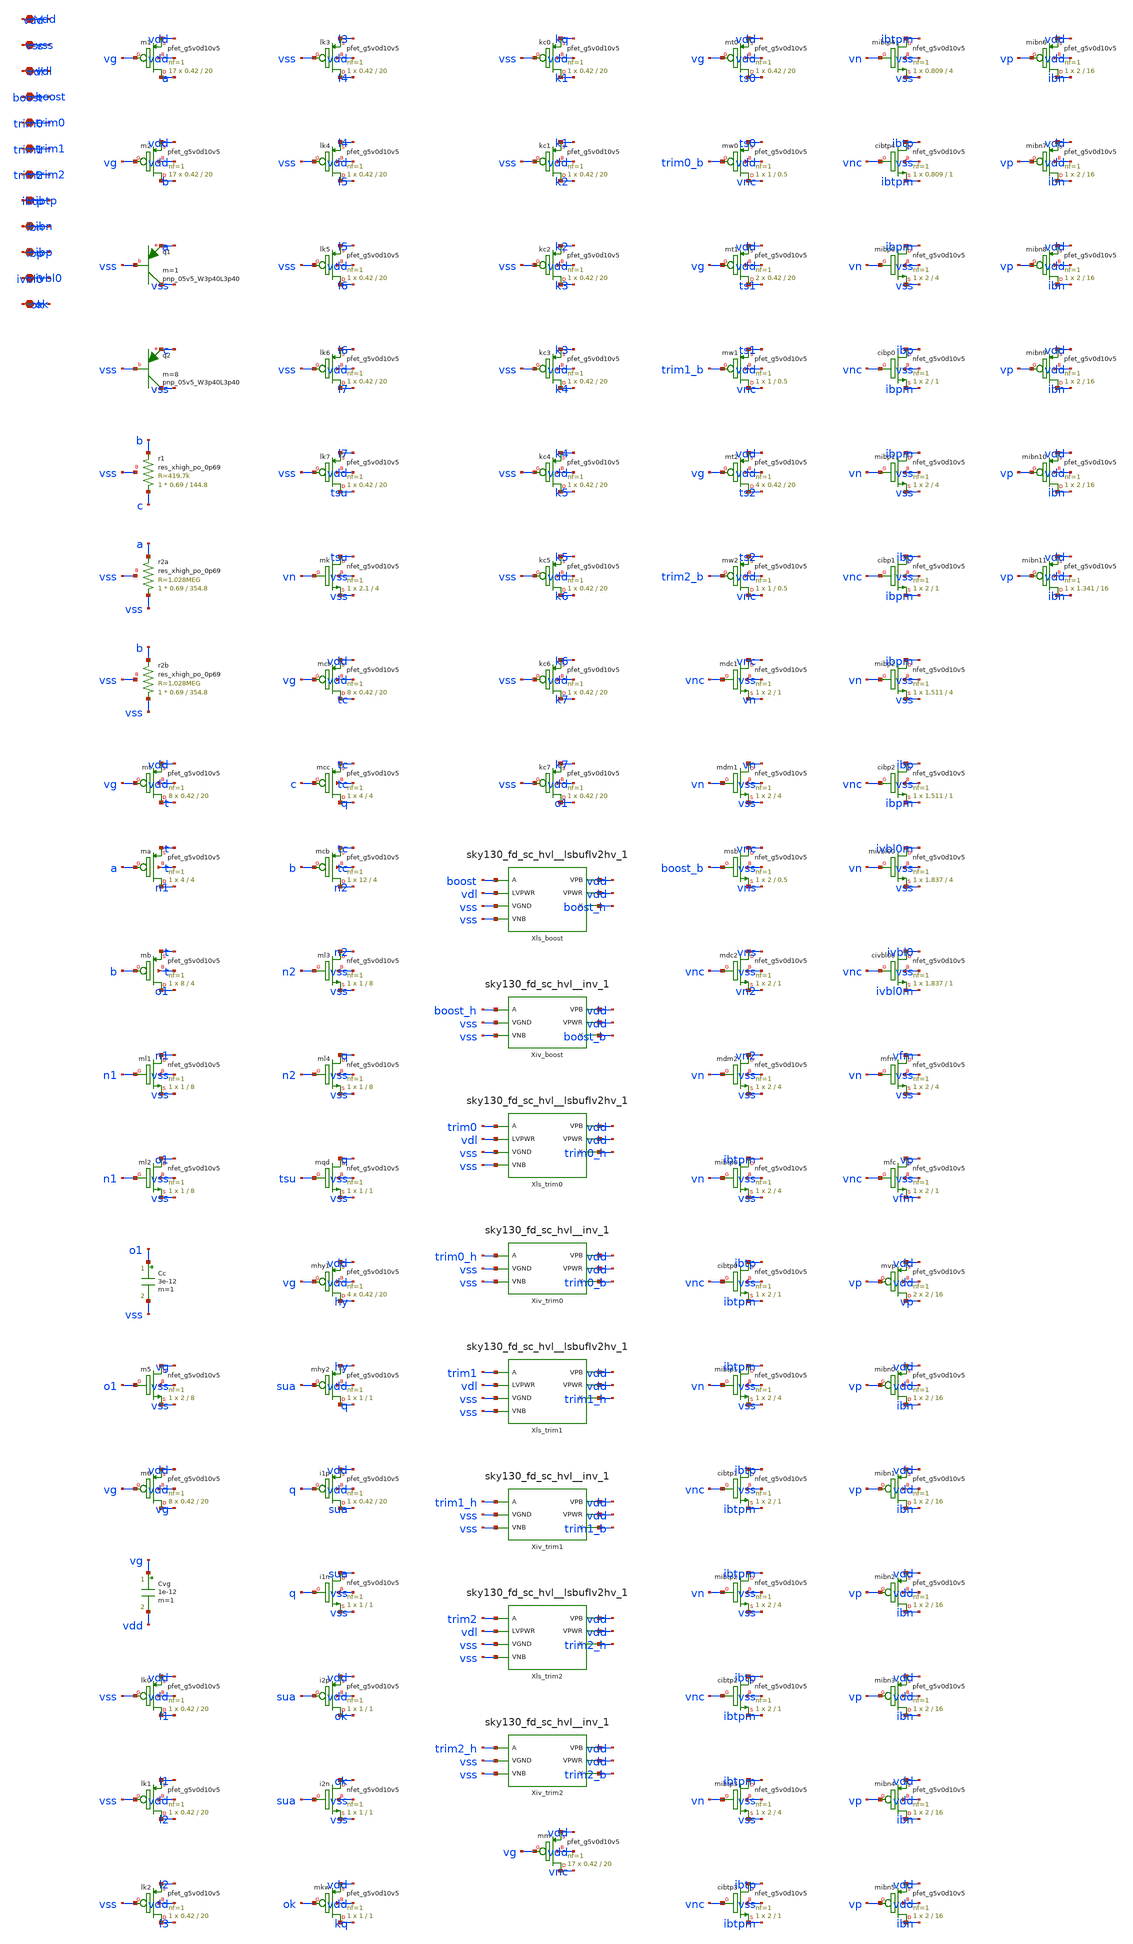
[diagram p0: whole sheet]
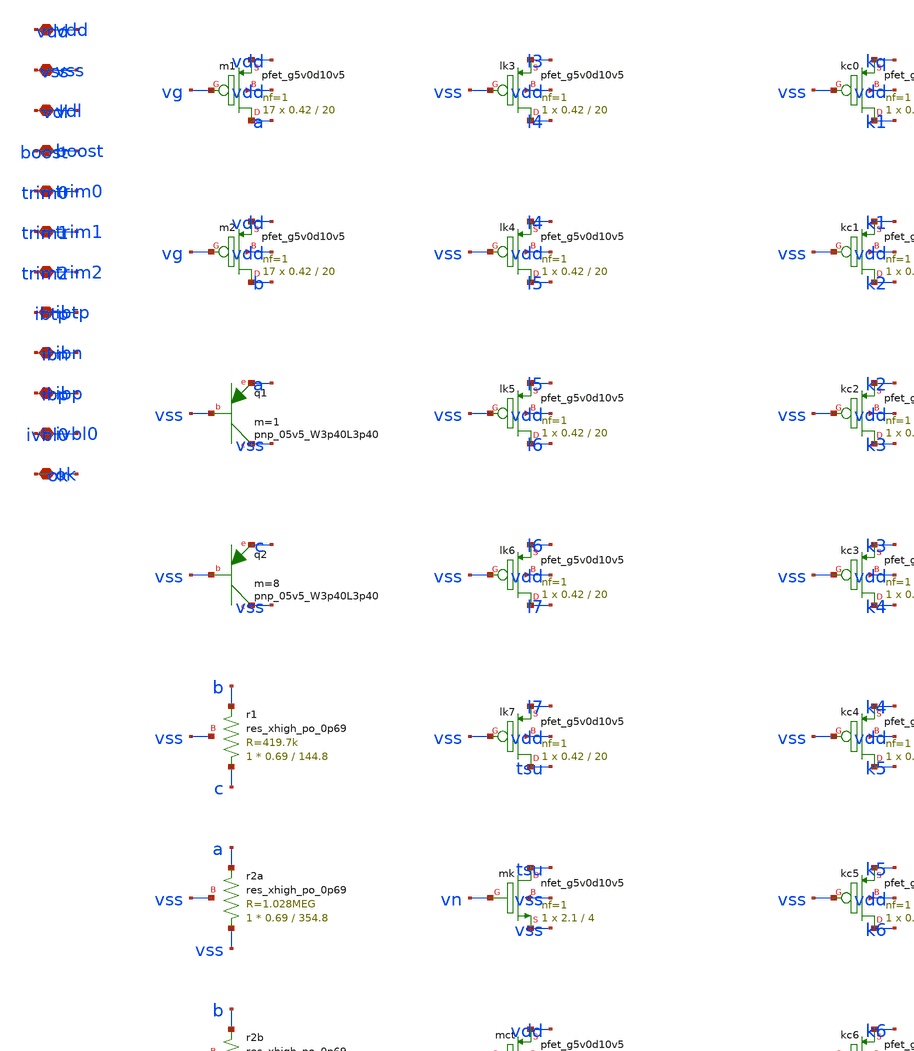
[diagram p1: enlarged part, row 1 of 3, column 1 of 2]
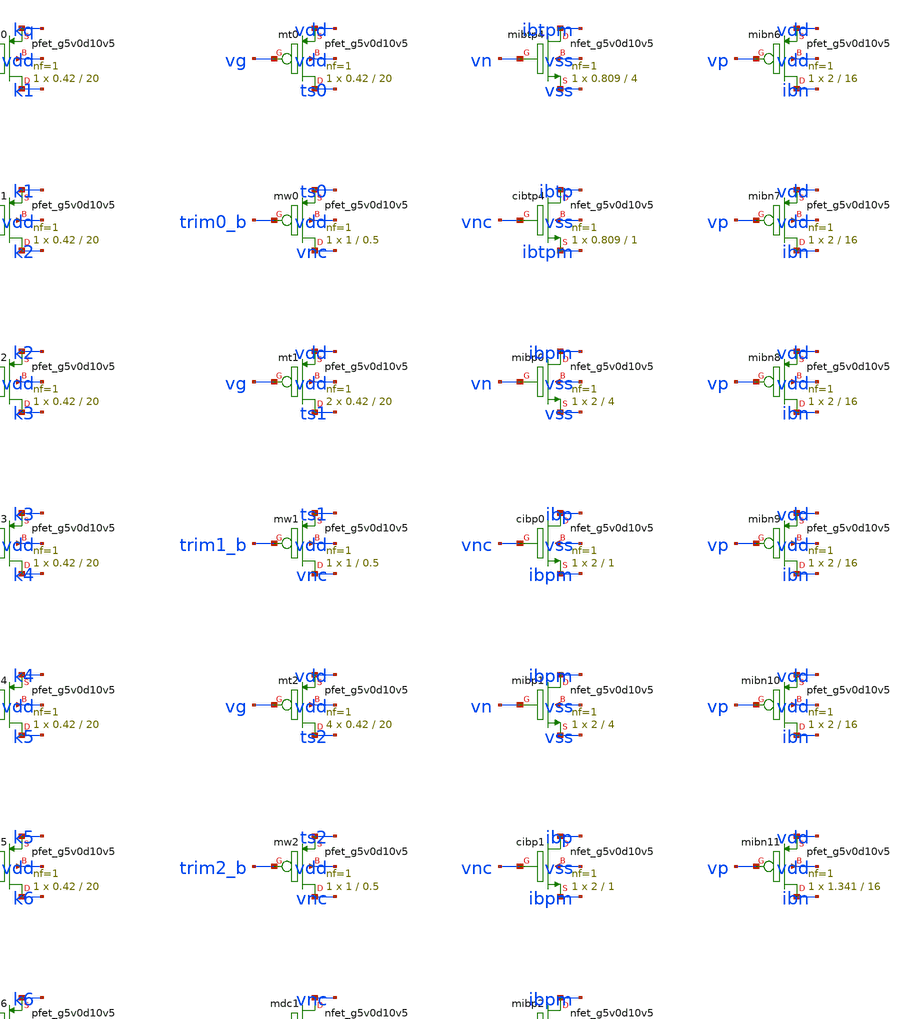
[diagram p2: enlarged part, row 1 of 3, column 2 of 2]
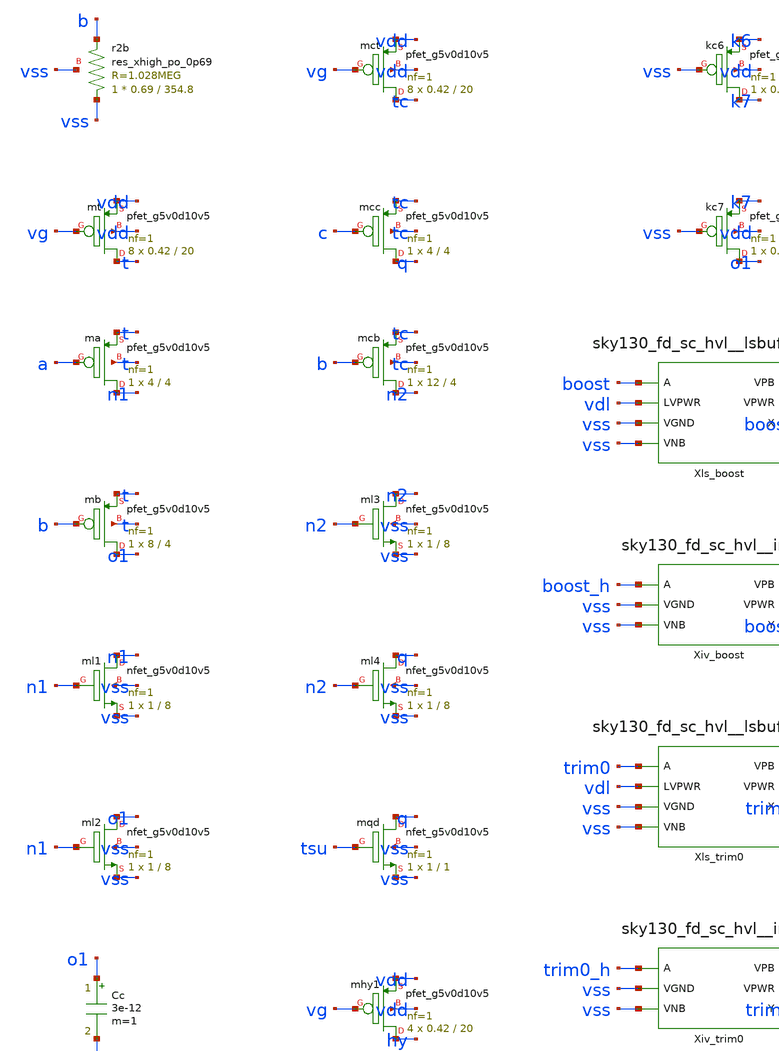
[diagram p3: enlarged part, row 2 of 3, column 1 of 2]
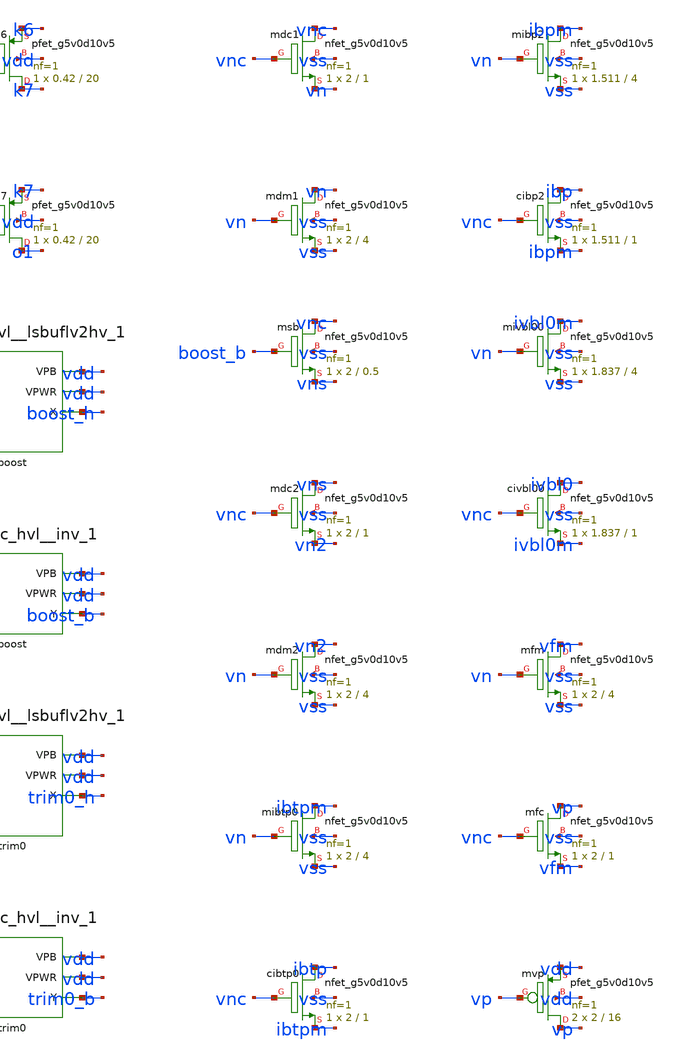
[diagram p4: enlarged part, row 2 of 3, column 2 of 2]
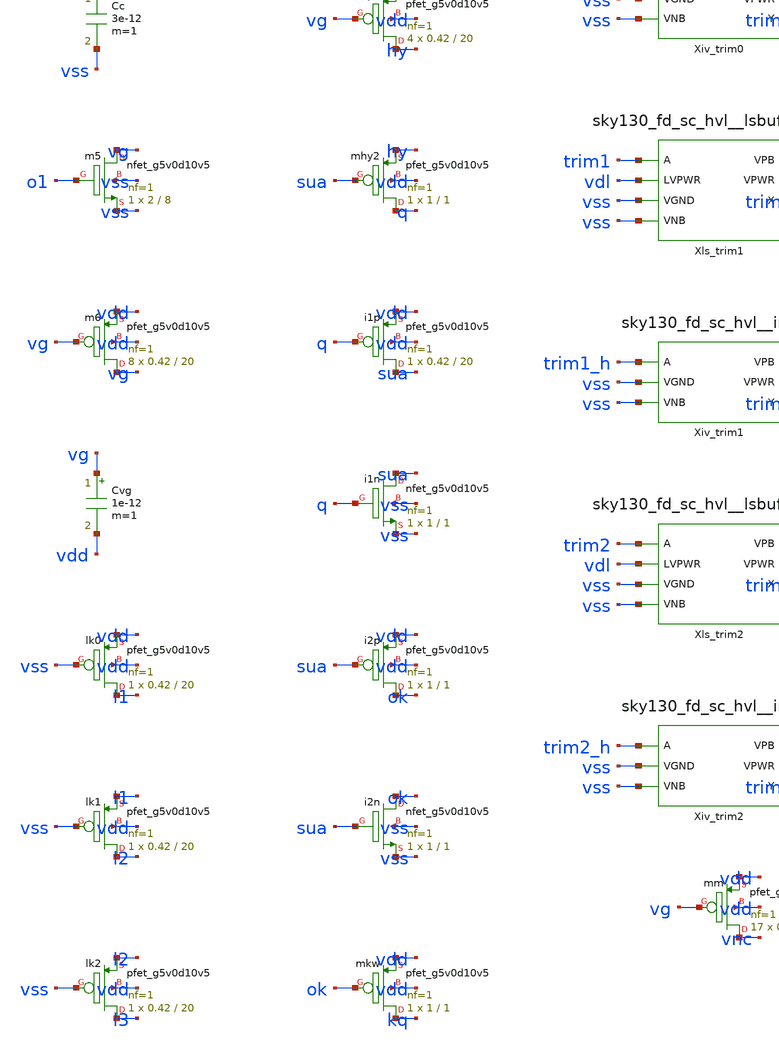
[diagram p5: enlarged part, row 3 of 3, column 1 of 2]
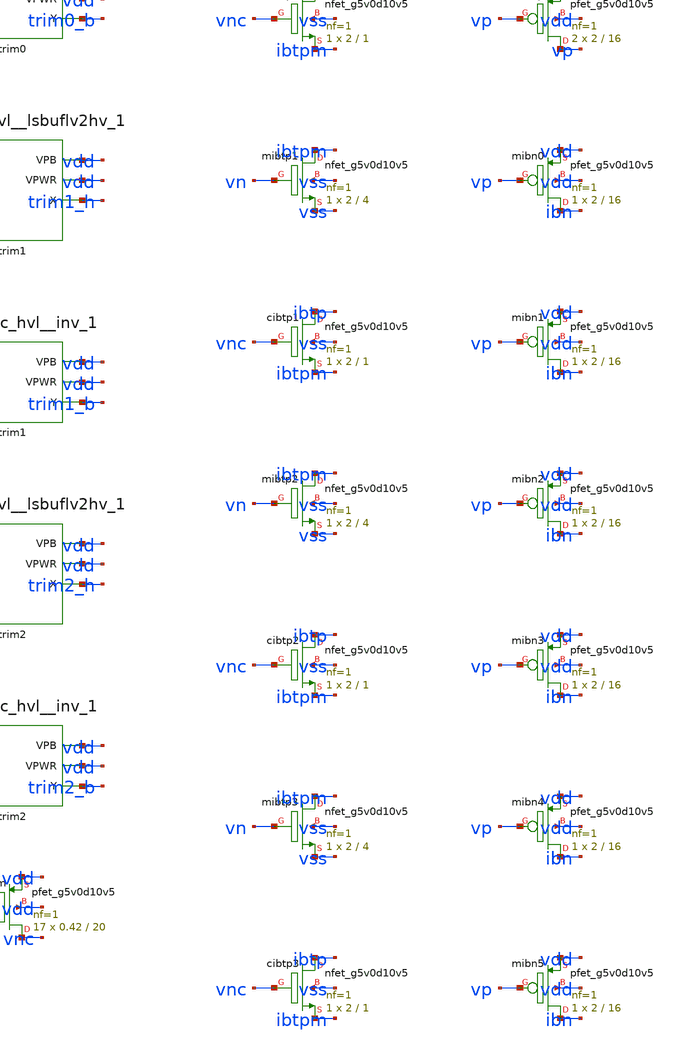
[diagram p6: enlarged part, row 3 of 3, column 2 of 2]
** sch_path: design/xschem/sch/c6_bias.sch
**.subckt c6_bias vdd vss vdl boost trim0 trim1 trim2 ibtp ibn ibp ivbl0 ok
*.iopin vdd
*.iopin vss
*.iopin vdl
*.iopin boost
*.iopin trim0
*.iopin trim1
*.iopin trim2
*.iopin ibtp
*.iopin ibn
*.iopin ibp
*.iopin ivbl0
*.iopin ok
Xm1 a vg vdd vdd sky130_fd_pr__pfet_g5v0d10v5 L=20 W=0.42 nf=1 ad='int((1 + 1)/2) * 0.42 / 1 * 0.29'
+ as='int((1 + 2)/2) * 0.42 / 1 * 0.29' pd='2*int((1 + 1)/2) * (0.42 / 1 + 0.29)' ps='2*int((1 + 2)/2) * (0.42 / 1 + 0.29)'
+ nrd='0.29 / 0.42 ' nrs='0.29 / 0.42 ' sa=0 sb=0 sd=0 mult=17 m=17
Xm2 b vg vdd vdd sky130_fd_pr__pfet_g5v0d10v5 L=20 W=0.42 nf=1 ad='int((1 + 1)/2) * 0.42 / 1 * 0.29'
+ as='int((1 + 2)/2) * 0.42 / 1 * 0.29' pd='2*int((1 + 1)/2) * (0.42 / 1 + 0.29)' ps='2*int((1 + 2)/2) * (0.42 / 1 + 0.29)'
+ nrd='0.29 / 0.42 ' nrs='0.29 / 0.42 ' sa=0 sb=0 sd=0 mult=17 m=17
Xq1 vss vss a sky130_fd_pr__pnp_05v5_W3p40L3p40 m=1
Xq2 vss vss c sky130_fd_pr__pnp_05v5_W3p40L3p40 m=8
Xr1 c b vss sky130_fd_pr__res_xhigh_po_0p69 L=144.8 mult=1 m=1
Xr2a vss a vss sky130_fd_pr__res_xhigh_po_0p69 L=354.8 mult=1 m=1
Xr2b vss b vss sky130_fd_pr__res_xhigh_po_0p69 L=354.8 mult=1 m=1
Xmt t vg vdd vdd sky130_fd_pr__pfet_g5v0d10v5 L=20 W=0.42 nf=1 ad='int((1 + 1)/2) * 0.42 / 1 * 0.29'
+ as='int((1 + 2)/2) * 0.42 / 1 * 0.29' pd='2*int((1 + 1)/2) * (0.42 / 1 + 0.29)' ps='2*int((1 + 2)/2) * (0.42 / 1 + 0.29)'
+ nrd='0.29 / 0.42 ' nrs='0.29 / 0.42 ' sa=0 sb=0 sd=0 mult=8 m=8
Xma n1 a t t sky130_fd_pr__pfet_g5v0d10v5 L=4 W=4 nf=1 ad='int((1 + 1)/2) * 4 / 1 * 0.29' as='int((1 + 2)/2) * 4 / 1 * 0.29'
+ pd='2*int((1 + 1)/2) * (4 / 1 + 0.29)' ps='2*int((1 + 2)/2) * (4 / 1 + 0.29)' nrd='0.29 / 4 ' nrs='0.29 / 4 '
+ sa=0 sb=0 sd=0 mult=1 m=1
Xmb o1 b t t sky130_fd_pr__pfet_g5v0d10v5 L=4 W=8 nf=1 ad='int((1 + 1)/2) * 8 / 1 * 0.29' as='int((1 + 2)/2) * 8 / 1 * 0.29'
+ pd='2*int((1 + 1)/2) * (8 / 1 + 0.29)' ps='2*int((1 + 2)/2) * (8 / 1 + 0.29)' nrd='0.29 / 8 ' nrs='0.29 / 8 '
+ sa=0 sb=0 sd=0 mult=1 m=1
Xml1 n1 n1 vss vss sky130_fd_pr__nfet_g5v0d10v5 L=8 W=1 nf=1 ad='int((1 + 1)/2) * 1 / 1 * 0.29' as='int((1 + 2)/2) * 1 / 1 * 0.29'
+ pd='2*int((1 + 1)/2) * (1 / 1 + 0.29)' ps='2*int((1 + 2)/2) * (1 / 1 + 0.29)' nrd='0.29 / 1 ' nrs='0.29 / 1 '
+ sa=0 sb=0 sd=0 mult=1 m=1
Xml2 o1 n1 vss vss sky130_fd_pr__nfet_g5v0d10v5 L=8 W=1 nf=1 ad='int((1 + 1)/2) * 1 / 1 * 0.29' as='int((1 + 2)/2) * 1 / 1 * 0.29'
+ pd='2*int((1 + 1)/2) * (1 / 1 + 0.29)' ps='2*int((1 + 2)/2) * (1 / 1 + 0.29)' nrd='0.29 / 1 ' nrs='0.29 / 1 '
+ sa=0 sb=0 sd=0 mult=1 m=1
Cc o1 vss 3e-12 m=1
Xm5 vg o1 vss vss sky130_fd_pr__nfet_g5v0d10v5 L=8 W=2 nf=1 ad='int((1 + 1)/2) * 2 / 1 * 0.29' as='int((1 + 2)/2) * 2 / 1 * 0.29'
+ pd='2*int((1 + 1)/2) * (2 / 1 + 0.29)' ps='2*int((1 + 2)/2) * (2 / 1 + 0.29)' nrd='0.29 / 2 ' nrs='0.29 / 2 '
+ sa=0 sb=0 sd=0 mult=1 m=1
Xm6 vg vg vdd vdd sky130_fd_pr__pfet_g5v0d10v5 L=20 W=0.42 nf=1 ad='int((1 + 1)/2) * 0.42 / 1 * 0.29'
+ as='int((1 + 2)/2) * 0.42 / 1 * 0.29' pd='2*int((1 + 1)/2) * (0.42 / 1 + 0.29)' ps='2*int((1 + 2)/2) * (0.42 / 1 + 0.29)'
+ nrd='0.29 / 0.42 ' nrs='0.29 / 0.42 ' sa=0 sb=0 sd=0 mult=8 m=8
Cvg vg vdd 1e-12 m=1
Xlk0 l1 vss vdd vdd sky130_fd_pr__pfet_g5v0d10v5 L=20 W=0.42 nf=1 ad='int((1 + 1)/2) * 0.42 / 1 * 0.29'
+ as='int((1 + 2)/2) * 0.42 / 1 * 0.29' pd='2*int((1 + 1)/2) * (0.42 / 1 + 0.29)' ps='2*int((1 + 2)/2) * (0.42 / 1 + 0.29)'
+ nrd='0.29 / 0.42 ' nrs='0.29 / 0.42 ' sa=0 sb=0 sd=0 mult=1 m=1
Xlk1 l2 vss l1 vdd sky130_fd_pr__pfet_g5v0d10v5 L=20 W=0.42 nf=1 ad='int((1 + 1)/2) * 0.42 / 1 * 0.29'
+ as='int((1 + 2)/2) * 0.42 / 1 * 0.29' pd='2*int((1 + 1)/2) * (0.42 / 1 + 0.29)' ps='2*int((1 + 2)/2) * (0.42 / 1 + 0.29)'
+ nrd='0.29 / 0.42 ' nrs='0.29 / 0.42 ' sa=0 sb=0 sd=0 mult=1 m=1
Xlk2 l3 vss l2 vdd sky130_fd_pr__pfet_g5v0d10v5 L=20 W=0.42 nf=1 ad='int((1 + 1)/2) * 0.42 / 1 * 0.29'
+ as='int((1 + 2)/2) * 0.42 / 1 * 0.29' pd='2*int((1 + 1)/2) * (0.42 / 1 + 0.29)' ps='2*int((1 + 2)/2) * (0.42 / 1 + 0.29)'
+ nrd='0.29 / 0.42 ' nrs='0.29 / 0.42 ' sa=0 sb=0 sd=0 mult=1 m=1
Xlk3 l4 vss l3 vdd sky130_fd_pr__pfet_g5v0d10v5 L=20 W=0.42 nf=1 ad='int((1 + 1)/2) * 0.42 / 1 * 0.29'
+ as='int((1 + 2)/2) * 0.42 / 1 * 0.29' pd='2*int((1 + 1)/2) * (0.42 / 1 + 0.29)' ps='2*int((1 + 2)/2) * (0.42 / 1 + 0.29)'
+ nrd='0.29 / 0.42 ' nrs='0.29 / 0.42 ' sa=0 sb=0 sd=0 mult=1 m=1
Xlk4 l5 vss l4 vdd sky130_fd_pr__pfet_g5v0d10v5 L=20 W=0.42 nf=1 ad='int((1 + 1)/2) * 0.42 / 1 * 0.29'
+ as='int((1 + 2)/2) * 0.42 / 1 * 0.29' pd='2*int((1 + 1)/2) * (0.42 / 1 + 0.29)' ps='2*int((1 + 2)/2) * (0.42 / 1 + 0.29)'
+ nrd='0.29 / 0.42 ' nrs='0.29 / 0.42 ' sa=0 sb=0 sd=0 mult=1 m=1
Xlk5 l6 vss l5 vdd sky130_fd_pr__pfet_g5v0d10v5 L=20 W=0.42 nf=1 ad='int((1 + 1)/2) * 0.42 / 1 * 0.29'
+ as='int((1 + 2)/2) * 0.42 / 1 * 0.29' pd='2*int((1 + 1)/2) * (0.42 / 1 + 0.29)' ps='2*int((1 + 2)/2) * (0.42 / 1 + 0.29)'
+ nrd='0.29 / 0.42 ' nrs='0.29 / 0.42 ' sa=0 sb=0 sd=0 mult=1 m=1
Xlk6 l7 vss l6 vdd sky130_fd_pr__pfet_g5v0d10v5 L=20 W=0.42 nf=1 ad='int((1 + 1)/2) * 0.42 / 1 * 0.29'
+ as='int((1 + 2)/2) * 0.42 / 1 * 0.29' pd='2*int((1 + 1)/2) * (0.42 / 1 + 0.29)' ps='2*int((1 + 2)/2) * (0.42 / 1 + 0.29)'
+ nrd='0.29 / 0.42 ' nrs='0.29 / 0.42 ' sa=0 sb=0 sd=0 mult=1 m=1
Xlk7 tsu vss l7 vdd sky130_fd_pr__pfet_g5v0d10v5 L=20 W=0.42 nf=1 ad='int((1 + 1)/2) * 0.42 / 1 * 0.29'
+ as='int((1 + 2)/2) * 0.42 / 1 * 0.29' pd='2*int((1 + 1)/2) * (0.42 / 1 + 0.29)' ps='2*int((1 + 2)/2) * (0.42 / 1 + 0.29)'
+ nrd='0.29 / 0.42 ' nrs='0.29 / 0.42 ' sa=0 sb=0 sd=0 mult=1 m=1
Xmk tsu vn vss vss sky130_fd_pr__nfet_g5v0d10v5 L=4 W=2.1 nf=1 ad='int((1 + 1)/2) * 2.1 / 1 * 0.29' as='int((1 + 2)/2) * 2.1 / 1 * 0.29'
+ pd='2*int((1 + 1)/2) * (2.1 / 1 + 0.29)' ps='2*int((1 + 2)/2) * (2.1 / 1 + 0.29)' nrd='0.29 / 2.1 ' nrs='0.29 / 2.1 '
+ sa=0 sb=0 sd=0 mult=1 m=1
Xmct tc vg vdd vdd sky130_fd_pr__pfet_g5v0d10v5 L=20 W=0.42 nf=1 ad='int((1 + 1)/2) * 0.42 / 1 * 0.29'
+ as='int((1 + 2)/2) * 0.42 / 1 * 0.29' pd='2*int((1 + 1)/2) * (0.42 / 1 + 0.29)' ps='2*int((1 + 2)/2) * (0.42 / 1 + 0.29)'
+ nrd='0.29 / 0.42 ' nrs='0.29 / 0.42 ' sa=0 sb=0 sd=0 mult=8 m=8
Xmcc q c tc tc sky130_fd_pr__pfet_g5v0d10v5 L=4 W=4 nf=1 ad='int((1 + 1)/2) * 4 / 1 * 0.29' as='int((1 + 2)/2) * 4 / 1 * 0.29'
+ pd='2*int((1 + 1)/2) * (4 / 1 + 0.29)' ps='2*int((1 + 2)/2) * (4 / 1 + 0.29)' nrd='0.29 / 4 ' nrs='0.29 / 4 '
+ sa=0 sb=0 sd=0 mult=1 m=1
Xmcb n2 b tc tc sky130_fd_pr__pfet_g5v0d10v5 L=4 W=12 nf=1 ad='int((1 + 1)/2) * 12 / 1 * 0.29' as='int((1 + 2)/2) * 12 / 1 * 0.29'
+ pd='2*int((1 + 1)/2) * (12 / 1 + 0.29)' ps='2*int((1 + 2)/2) * (12 / 1 + 0.29)' nrd='0.29 / 12 ' nrs='0.29 / 12 '
+ sa=0 sb=0 sd=0 mult=1 m=1
Xml3 n2 n2 vss vss sky130_fd_pr__nfet_g5v0d10v5 L=8 W=1 nf=1 ad='int((1 + 1)/2) * 1 / 1 * 0.29' as='int((1 + 2)/2) * 1 / 1 * 0.29'
+ pd='2*int((1 + 1)/2) * (1 / 1 + 0.29)' ps='2*int((1 + 2)/2) * (1 / 1 + 0.29)' nrd='0.29 / 1 ' nrs='0.29 / 1 '
+ sa=0 sb=0 sd=0 mult=1 m=1
Xml4 q n2 vss vss sky130_fd_pr__nfet_g5v0d10v5 L=8 W=1 nf=1 ad='int((1 + 1)/2) * 1 / 1 * 0.29' as='int((1 + 2)/2) * 1 / 1 * 0.29'
+ pd='2*int((1 + 1)/2) * (1 / 1 + 0.29)' ps='2*int((1 + 2)/2) * (1 / 1 + 0.29)' nrd='0.29 / 1 ' nrs='0.29 / 1 '
+ sa=0 sb=0 sd=0 mult=1 m=1
Xmqd q tsu vss vss sky130_fd_pr__nfet_g5v0d10v5 L=1 W=1 nf=1 ad='int((1 + 1)/2) * 1 / 1 * 0.29' as='int((1 + 2)/2) * 1 / 1 * 0.29'
+ pd='2*int((1 + 1)/2) * (1 / 1 + 0.29)' ps='2*int((1 + 2)/2) * (1 / 1 + 0.29)' nrd='0.29 / 1 ' nrs='0.29 / 1 '
+ sa=0 sb=0 sd=0 mult=1 m=1
Xmhy1 hy vg vdd vdd sky130_fd_pr__pfet_g5v0d10v5 L=20 W=0.42 nf=1 ad='int((1 + 1)/2) * 0.42 / 1 * 0.29'
+ as='int((1 + 2)/2) * 0.42 / 1 * 0.29' pd='2*int((1 + 1)/2) * (0.42 / 1 + 0.29)' ps='2*int((1 + 2)/2) * (0.42 / 1 + 0.29)'
+ nrd='0.29 / 0.42 ' nrs='0.29 / 0.42 ' sa=0 sb=0 sd=0 mult=4 m=4
Xmhy2 q sua hy vdd sky130_fd_pr__pfet_g5v0d10v5 L=1 W=1 nf=1 ad='int((1 + 1)/2) * 1 / 1 * 0.29' as='int((1 + 2)/2) * 1 / 1 * 0.29'
+ pd='2*int((1 + 1)/2) * (1 / 1 + 0.29)' ps='2*int((1 + 2)/2) * (1 / 1 + 0.29)' nrd='0.29 / 1 ' nrs='0.29 / 1 '
+ sa=0 sb=0 sd=0 mult=1 m=1
Xi1p sua q vdd vdd sky130_fd_pr__pfet_g5v0d10v5 L=20 W=0.42 nf=1 ad='int((1 + 1)/2) * 0.42 / 1 * 0.29'
+ as='int((1 + 2)/2) * 0.42 / 1 * 0.29' pd='2*int((1 + 1)/2) * (0.42 / 1 + 0.29)' ps='2*int((1 + 2)/2) * (0.42 / 1 + 0.29)'
+ nrd='0.29 / 0.42 ' nrs='0.29 / 0.42 ' sa=0 sb=0 sd=0 mult=1 m=1
Xi1n sua q vss vss sky130_fd_pr__nfet_g5v0d10v5 L=1 W=1 nf=1 ad='int((1 + 1)/2) * 1 / 1 * 0.29' as='int((1 + 2)/2) * 1 / 1 * 0.29'
+ pd='2*int((1 + 1)/2) * (1 / 1 + 0.29)' ps='2*int((1 + 2)/2) * (1 / 1 + 0.29)' nrd='0.29 / 1 ' nrs='0.29 / 1 '
+ sa=0 sb=0 sd=0 mult=1 m=1
Xi2p ok sua vdd vdd sky130_fd_pr__pfet_g5v0d10v5 L=1 W=1 nf=1 ad='int((1 + 1)/2) * 1 / 1 * 0.29' as='int((1 + 2)/2) * 1 / 1 * 0.29'
+ pd='2*int((1 + 1)/2) * (1 / 1 + 0.29)' ps='2*int((1 + 2)/2) * (1 / 1 + 0.29)' nrd='0.29 / 1 ' nrs='0.29 / 1 '
+ sa=0 sb=0 sd=0 mult=1 m=1
Xi2n ok sua vss vss sky130_fd_pr__nfet_g5v0d10v5 L=1 W=1 nf=1 ad='int((1 + 1)/2) * 1 / 1 * 0.29' as='int((1 + 2)/2) * 1 / 1 * 0.29'
+ pd='2*int((1 + 1)/2) * (1 / 1 + 0.29)' ps='2*int((1 + 2)/2) * (1 / 1 + 0.29)' nrd='0.29 / 1 ' nrs='0.29 / 1 '
+ sa=0 sb=0 sd=0 mult=1 m=1
Xmkw kq ok vdd vdd sky130_fd_pr__pfet_g5v0d10v5 L=1 W=1 nf=1 ad='int((1 + 1)/2) * 1 / 1 * 0.29' as='int((1 + 2)/2) * 1 / 1 * 0.29'
+ pd='2*int((1 + 1)/2) * (1 / 1 + 0.29)' ps='2*int((1 + 2)/2) * (1 / 1 + 0.29)' nrd='0.29 / 1 ' nrs='0.29 / 1 '
+ sa=0 sb=0 sd=0 mult=1 m=1
Xkc0 k1 vss kq vdd sky130_fd_pr__pfet_g5v0d10v5 L=20 W=0.42 nf=1 ad='int((1 + 1)/2) * 0.42 / 1 * 0.29'
+ as='int((1 + 2)/2) * 0.42 / 1 * 0.29' pd='2*int((1 + 1)/2) * (0.42 / 1 + 0.29)' ps='2*int((1 + 2)/2) * (0.42 / 1 + 0.29)'
+ nrd='0.29 / 0.42 ' nrs='0.29 / 0.42 ' sa=0 sb=0 sd=0 mult=1 m=1
Xkc1 k2 vss k1 vdd sky130_fd_pr__pfet_g5v0d10v5 L=20 W=0.42 nf=1 ad='int((1 + 1)/2) * 0.42 / 1 * 0.29'
+ as='int((1 + 2)/2) * 0.42 / 1 * 0.29' pd='2*int((1 + 1)/2) * (0.42 / 1 + 0.29)' ps='2*int((1 + 2)/2) * (0.42 / 1 + 0.29)'
+ nrd='0.29 / 0.42 ' nrs='0.29 / 0.42 ' sa=0 sb=0 sd=0 mult=1 m=1
Xkc2 k3 vss k2 vdd sky130_fd_pr__pfet_g5v0d10v5 L=20 W=0.42 nf=1 ad='int((1 + 1)/2) * 0.42 / 1 * 0.29'
+ as='int((1 + 2)/2) * 0.42 / 1 * 0.29' pd='2*int((1 + 1)/2) * (0.42 / 1 + 0.29)' ps='2*int((1 + 2)/2) * (0.42 / 1 + 0.29)'
+ nrd='0.29 / 0.42 ' nrs='0.29 / 0.42 ' sa=0 sb=0 sd=0 mult=1 m=1
Xkc3 k4 vss k3 vdd sky130_fd_pr__pfet_g5v0d10v5 L=20 W=0.42 nf=1 ad='int((1 + 1)/2) * 0.42 / 1 * 0.29'
+ as='int((1 + 2)/2) * 0.42 / 1 * 0.29' pd='2*int((1 + 1)/2) * (0.42 / 1 + 0.29)' ps='2*int((1 + 2)/2) * (0.42 / 1 + 0.29)'
+ nrd='0.29 / 0.42 ' nrs='0.29 / 0.42 ' sa=0 sb=0 sd=0 mult=1 m=1
Xkc4 k5 vss k4 vdd sky130_fd_pr__pfet_g5v0d10v5 L=20 W=0.42 nf=1 ad='int((1 + 1)/2) * 0.42 / 1 * 0.29'
+ as='int((1 + 2)/2) * 0.42 / 1 * 0.29' pd='2*int((1 + 1)/2) * (0.42 / 1 + 0.29)' ps='2*int((1 + 2)/2) * (0.42 / 1 + 0.29)'
+ nrd='0.29 / 0.42 ' nrs='0.29 / 0.42 ' sa=0 sb=0 sd=0 mult=1 m=1
Xkc5 k6 vss k5 vdd sky130_fd_pr__pfet_g5v0d10v5 L=20 W=0.42 nf=1 ad='int((1 + 1)/2) * 0.42 / 1 * 0.29'
+ as='int((1 + 2)/2) * 0.42 / 1 * 0.29' pd='2*int((1 + 1)/2) * (0.42 / 1 + 0.29)' ps='2*int((1 + 2)/2) * (0.42 / 1 + 0.29)'
+ nrd='0.29 / 0.42 ' nrs='0.29 / 0.42 ' sa=0 sb=0 sd=0 mult=1 m=1
Xkc6 k7 vss k6 vdd sky130_fd_pr__pfet_g5v0d10v5 L=20 W=0.42 nf=1 ad='int((1 + 1)/2) * 0.42 / 1 * 0.29'
+ as='int((1 + 2)/2) * 0.42 / 1 * 0.29' pd='2*int((1 + 1)/2) * (0.42 / 1 + 0.29)' ps='2*int((1 + 2)/2) * (0.42 / 1 + 0.29)'
+ nrd='0.29 / 0.42 ' nrs='0.29 / 0.42 ' sa=0 sb=0 sd=0 mult=1 m=1
Xkc7 o1 vss k7 vdd sky130_fd_pr__pfet_g5v0d10v5 L=20 W=0.42 nf=1 ad='int((1 + 1)/2) * 0.42 / 1 * 0.29'
+ as='int((1 + 2)/2) * 0.42 / 1 * 0.29' pd='2*int((1 + 1)/2) * (0.42 / 1 + 0.29)' ps='2*int((1 + 2)/2) * (0.42 / 1 + 0.29)'
+ nrd='0.29 / 0.42 ' nrs='0.29 / 0.42 ' sa=0 sb=0 sd=0 mult=1 m=1
Xls_boost boost vdl vss vss vdd vdd boost_h sky130_fd_sc_hvl__lsbuflv2hv_1
Xiv_boost boost_h vss vss vdd vdd boost_b sky130_fd_sc_hvl__inv_1
Xls_trim0 trim0 vdl vss vss vdd vdd trim0_h sky130_fd_sc_hvl__lsbuflv2hv_1
Xiv_trim0 trim0_h vss vss vdd vdd trim0_b sky130_fd_sc_hvl__inv_1
Xls_trim1 trim1 vdl vss vss vdd vdd trim1_h sky130_fd_sc_hvl__lsbuflv2hv_1
Xiv_trim1 trim1_h vss vss vdd vdd trim1_b sky130_fd_sc_hvl__inv_1
Xls_trim2 trim2 vdl vss vss vdd vdd trim2_h sky130_fd_sc_hvl__lsbuflv2hv_1
Xiv_trim2 trim2_h vss vss vdd vdd trim2_b sky130_fd_sc_hvl__inv_1
Xmm vnc vg vdd vdd sky130_fd_pr__pfet_g5v0d10v5 L=20 W=0.42 nf=1 ad='int((1 + 1)/2) * 0.42 / 1 * 0.29'
+ as='int((1 + 2)/2) * 0.42 / 1 * 0.29' pd='2*int((1 + 1)/2) * (0.42 / 1 + 0.29)' ps='2*int((1 + 2)/2) * (0.42 / 1 + 0.29)'
+ nrd='0.29 / 0.42 ' nrs='0.29 / 0.42 ' sa=0 sb=0 sd=0 mult=17 m=17
Xmt0 ts0 vg vdd vdd sky130_fd_pr__pfet_g5v0d10v5 L=20 W=0.42 nf=1 ad='int((1 + 1)/2) * 0.42 / 1 * 0.29'
+ as='int((1 + 2)/2) * 0.42 / 1 * 0.29' pd='2*int((1 + 1)/2) * (0.42 / 1 + 0.29)' ps='2*int((1 + 2)/2) * (0.42 / 1 + 0.29)'
+ nrd='0.29 / 0.42 ' nrs='0.29 / 0.42 ' sa=0 sb=0 sd=0 mult=1 m=1
Xmw0 vnc trim0_b ts0 vdd sky130_fd_pr__pfet_g5v0d10v5 L=0.5 W=1 nf=1 ad='int((1 + 1)/2) * 1 / 1 * 0.29'
+ as='int((1 + 2)/2) * 1 / 1 * 0.29' pd='2*int((1 + 1)/2) * (1 / 1 + 0.29)' ps='2*int((1 + 2)/2) * (1 / 1 + 0.29)'
+ nrd='0.29 / 1 ' nrs='0.29 / 1 ' sa=0 sb=0 sd=0 mult=1 m=1
Xmt1 ts1 vg vdd vdd sky130_fd_pr__pfet_g5v0d10v5 L=20 W=0.42 nf=1 ad='int((1 + 1)/2) * 0.42 / 1 * 0.29'
+ as='int((1 + 2)/2) * 0.42 / 1 * 0.29' pd='2*int((1 + 1)/2) * (0.42 / 1 + 0.29)' ps='2*int((1 + 2)/2) * (0.42 / 1 + 0.29)'
+ nrd='0.29 / 0.42 ' nrs='0.29 / 0.42 ' sa=0 sb=0 sd=0 mult=2 m=2
Xmw1 vnc trim1_b ts1 vdd sky130_fd_pr__pfet_g5v0d10v5 L=0.5 W=1 nf=1 ad='int((1 + 1)/2) * 1 / 1 * 0.29'
+ as='int((1 + 2)/2) * 1 / 1 * 0.29' pd='2*int((1 + 1)/2) * (1 / 1 + 0.29)' ps='2*int((1 + 2)/2) * (1 / 1 + 0.29)'
+ nrd='0.29 / 1 ' nrs='0.29 / 1 ' sa=0 sb=0 sd=0 mult=1 m=1
Xmt2 ts2 vg vdd vdd sky130_fd_pr__pfet_g5v0d10v5 L=20 W=0.42 nf=1 ad='int((1 + 1)/2) * 0.42 / 1 * 0.29'
+ as='int((1 + 2)/2) * 0.42 / 1 * 0.29' pd='2*int((1 + 1)/2) * (0.42 / 1 + 0.29)' ps='2*int((1 + 2)/2) * (0.42 / 1 + 0.29)'
+ nrd='0.29 / 0.42 ' nrs='0.29 / 0.42 ' sa=0 sb=0 sd=0 mult=4 m=4
Xmw2 vnc trim2_b ts2 vdd sky130_fd_pr__pfet_g5v0d10v5 L=0.5 W=1 nf=1 ad='int((1 + 1)/2) * 1 / 1 * 0.29'
+ as='int((1 + 2)/2) * 1 / 1 * 0.29' pd='2*int((1 + 1)/2) * (1 / 1 + 0.29)' ps='2*int((1 + 2)/2) * (1 / 1 + 0.29)'
+ nrd='0.29 / 1 ' nrs='0.29 / 1 ' sa=0 sb=0 sd=0 mult=1 m=1
Xmdc1 vnc vnc vn vss sky130_fd_pr__nfet_g5v0d10v5 L=1 W=2 nf=1 ad='int((1 + 1)/2) * 2 / 1 * 0.29' as='int((1 + 2)/2) * 2 / 1 * 0.29'
+ pd='2*int((1 + 1)/2) * (2 / 1 + 0.29)' ps='2*int((1 + 2)/2) * (2 / 1 + 0.29)' nrd='0.29 / 2 ' nrs='0.29 / 2 '
+ sa=0 sb=0 sd=0 mult=1 m=1
Xmdm1 vn vn vss vss sky130_fd_pr__nfet_g5v0d10v5 L=4 W=2 nf=1 ad='int((1 + 1)/2) * 2 / 1 * 0.29' as='int((1 + 2)/2) * 2 / 1 * 0.29'
+ pd='2*int((1 + 1)/2) * (2 / 1 + 0.29)' ps='2*int((1 + 2)/2) * (2 / 1 + 0.29)' nrd='0.29 / 2 ' nrs='0.29 / 2 '
+ sa=0 sb=0 sd=0 mult=1 m=1
Xmsb vnc boost_b vns vss sky130_fd_pr__nfet_g5v0d10v5 L=0.5 W=2 nf=1 ad='int((1 + 1)/2) * 2 / 1 * 0.29'
+ as='int((1 + 2)/2) * 2 / 1 * 0.29' pd='2*int((1 + 1)/2) * (2 / 1 + 0.29)' ps='2*int((1 + 2)/2) * (2 / 1 + 0.29)'
+ nrd='0.29 / 2 ' nrs='0.29 / 2 ' sa=0 sb=0 sd=0 mult=1 m=1
Xmdc2 vns vnc vn2 vss sky130_fd_pr__nfet_g5v0d10v5 L=1 W=2 nf=1 ad='int((1 + 1)/2) * 2 / 1 * 0.29' as='int((1 + 2)/2) * 2 / 1 * 0.29'
+ pd='2*int((1 + 1)/2) * (2 / 1 + 0.29)' ps='2*int((1 + 2)/2) * (2 / 1 + 0.29)' nrd='0.29 / 2 ' nrs='0.29 / 2 '
+ sa=0 sb=0 sd=0 mult=1 m=1
Xmdm2 vn2 vn vss vss sky130_fd_pr__nfet_g5v0d10v5 L=4 W=2 nf=1 ad='int((1 + 1)/2) * 2 / 1 * 0.29' as='int((1 + 2)/2) * 2 / 1 * 0.29'
+ pd='2*int((1 + 1)/2) * (2 / 1 + 0.29)' ps='2*int((1 + 2)/2) * (2 / 1 + 0.29)' nrd='0.29 / 2 ' nrs='0.29 / 2 '
+ sa=0 sb=0 sd=0 mult=1 m=1
Xmibtp0 ibtpm vn vss vss sky130_fd_pr__nfet_g5v0d10v5 L=4 W=2 nf=1 ad='int((1 + 1)/2) * 2 / 1 * 0.29'
+ as='int((1 + 2)/2) * 2 / 1 * 0.29' pd='2*int((1 + 1)/2) * (2 / 1 + 0.29)' ps='2*int((1 + 2)/2) * (2 / 1 + 0.29)'
+ nrd='0.29 / 2 ' nrs='0.29 / 2 ' sa=0 sb=0 sd=0 mult=1 m=1
Xcibtp0 ibtp vnc ibtpm vss sky130_fd_pr__nfet_g5v0d10v5 L=1 W=2 nf=1 ad='int((1 + 1)/2) * 2 / 1 * 0.29'
+ as='int((1 + 2)/2) * 2 / 1 * 0.29' pd='2*int((1 + 1)/2) * (2 / 1 + 0.29)' ps='2*int((1 + 2)/2) * (2 / 1 + 0.29)'
+ nrd='0.29 / 2 ' nrs='0.29 / 2 ' sa=0 sb=0 sd=0 mult=1 m=1
Xmibtp1 ibtpm vn vss vss sky130_fd_pr__nfet_g5v0d10v5 L=4 W=2 nf=1 ad='int((1 + 1)/2) * 2 / 1 * 0.29'
+ as='int((1 + 2)/2) * 2 / 1 * 0.29' pd='2*int((1 + 1)/2) * (2 / 1 + 0.29)' ps='2*int((1 + 2)/2) * (2 / 1 + 0.29)'
+ nrd='0.29 / 2 ' nrs='0.29 / 2 ' sa=0 sb=0 sd=0 mult=1 m=1
Xcibtp1 ibtp vnc ibtpm vss sky130_fd_pr__nfet_g5v0d10v5 L=1 W=2 nf=1 ad='int((1 + 1)/2) * 2 / 1 * 0.29'
+ as='int((1 + 2)/2) * 2 / 1 * 0.29' pd='2*int((1 + 1)/2) * (2 / 1 + 0.29)' ps='2*int((1 + 2)/2) * (2 / 1 + 0.29)'
+ nrd='0.29 / 2 ' nrs='0.29 / 2 ' sa=0 sb=0 sd=0 mult=1 m=1
Xmibtp2 ibtpm vn vss vss sky130_fd_pr__nfet_g5v0d10v5 L=4 W=2 nf=1 ad='int((1 + 1)/2) * 2 / 1 * 0.29'
+ as='int((1 + 2)/2) * 2 / 1 * 0.29' pd='2*int((1 + 1)/2) * (2 / 1 + 0.29)' ps='2*int((1 + 2)/2) * (2 / 1 + 0.29)'
+ nrd='0.29 / 2 ' nrs='0.29 / 2 ' sa=0 sb=0 sd=0 mult=1 m=1
Xcibtp2 ibtp vnc ibtpm vss sky130_fd_pr__nfet_g5v0d10v5 L=1 W=2 nf=1 ad='int((1 + 1)/2) * 2 / 1 * 0.29'
+ as='int((1 + 2)/2) * 2 / 1 * 0.29' pd='2*int((1 + 1)/2) * (2 / 1 + 0.29)' ps='2*int((1 + 2)/2) * (2 / 1 + 0.29)'
+ nrd='0.29 / 2 ' nrs='0.29 / 2 ' sa=0 sb=0 sd=0 mult=1 m=1
Xmibtp3 ibtpm vn vss vss sky130_fd_pr__nfet_g5v0d10v5 L=4 W=2 nf=1 ad='int((1 + 1)/2) * 2 / 1 * 0.29'
+ as='int((1 + 2)/2) * 2 / 1 * 0.29' pd='2*int((1 + 1)/2) * (2 / 1 + 0.29)' ps='2*int((1 + 2)/2) * (2 / 1 + 0.29)'
+ nrd='0.29 / 2 ' nrs='0.29 / 2 ' sa=0 sb=0 sd=0 mult=1 m=1
Xcibtp3 ibtp vnc ibtpm vss sky130_fd_pr__nfet_g5v0d10v5 L=1 W=2 nf=1 ad='int((1 + 1)/2) * 2 / 1 * 0.29'
+ as='int((1 + 2)/2) * 2 / 1 * 0.29' pd='2*int((1 + 1)/2) * (2 / 1 + 0.29)' ps='2*int((1 + 2)/2) * (2 / 1 + 0.29)'
+ nrd='0.29 / 2 ' nrs='0.29 / 2 ' sa=0 sb=0 sd=0 mult=1 m=1
Xmibtp4 ibtpm vn vss vss sky130_fd_pr__nfet_g5v0d10v5 L=4 W=0.809 nf=1 ad='int((1 + 1)/2) * 0.809 / 1 * 0.29'
+ as='int((1 + 2)/2) * 0.809 / 1 * 0.29' pd='2*int((1 + 1)/2) * (0.809 / 1 + 0.29)' ps='2*int((1 + 2)/2) * (0.809 / 1 + 0.29)'
+ nrd='0.29 / 0.809 ' nrs='0.29 / 0.809 ' sa=0 sb=0 sd=0 mult=1 m=1
Xcibtp4 ibtp vnc ibtpm vss sky130_fd_pr__nfet_g5v0d10v5 L=1 W=0.809 nf=1 ad='int((1 + 1)/2) * 0.809 / 1 * 0.29'
+ as='int((1 + 2)/2) * 0.809 / 1 * 0.29' pd='2*int((1 + 1)/2) * (0.809 / 1 + 0.29)' ps='2*int((1 + 2)/2) * (0.809 / 1 + 0.29)'
+ nrd='0.29 / 0.809 ' nrs='0.29 / 0.809 ' sa=0 sb=0 sd=0 mult=1 m=1
Xmibp0 ibpm vn vss vss sky130_fd_pr__nfet_g5v0d10v5 L=4 W=2 nf=1 ad='int((1 + 1)/2) * 2 / 1 * 0.29' as='int((1 + 2)/2) * 2 / 1 * 0.29'
+ pd='2*int((1 + 1)/2) * (2 / 1 + 0.29)' ps='2*int((1 + 2)/2) * (2 / 1 + 0.29)' nrd='0.29 / 2 ' nrs='0.29 / 2 '
+ sa=0 sb=0 sd=0 mult=1 m=1
Xcibp0 ibp vnc ibpm vss sky130_fd_pr__nfet_g5v0d10v5 L=1 W=2 nf=1 ad='int((1 + 1)/2) * 2 / 1 * 0.29'
+ as='int((1 + 2)/2) * 2 / 1 * 0.29' pd='2*int((1 + 1)/2) * (2 / 1 + 0.29)' ps='2*int((1 + 2)/2) * (2 / 1 + 0.29)'
+ nrd='0.29 / 2 ' nrs='0.29 / 2 ' sa=0 sb=0 sd=0 mult=1 m=1
Xmibp1 ibpm vn vss vss sky130_fd_pr__nfet_g5v0d10v5 L=4 W=2 nf=1 ad='int((1 + 1)/2) * 2 / 1 * 0.29' as='int((1 + 2)/2) * 2 / 1 * 0.29'
+ pd='2*int((1 + 1)/2) * (2 / 1 + 0.29)' ps='2*int((1 + 2)/2) * (2 / 1 + 0.29)' nrd='0.29 / 2 ' nrs='0.29 / 2 '
+ sa=0 sb=0 sd=0 mult=1 m=1
Xcibp1 ibp vnc ibpm vss sky130_fd_pr__nfet_g5v0d10v5 L=1 W=2 nf=1 ad='int((1 + 1)/2) * 2 / 1 * 0.29'
+ as='int((1 + 2)/2) * 2 / 1 * 0.29' pd='2*int((1 + 1)/2) * (2 / 1 + 0.29)' ps='2*int((1 + 2)/2) * (2 / 1 + 0.29)'
+ nrd='0.29 / 2 ' nrs='0.29 / 2 ' sa=0 sb=0 sd=0 mult=1 m=1
Xmibp2 ibpm vn vss vss sky130_fd_pr__nfet_g5v0d10v5 L=4 W=1.511 nf=1 ad='int((1 + 1)/2) * 1.511 / 1 * 0.29'
+ as='int((1 + 2)/2) * 1.511 / 1 * 0.29' pd='2*int((1 + 1)/2) * (1.511 / 1 + 0.29)' ps='2*int((1 + 2)/2) * (1.511 / 1 + 0.29)'
+ nrd='0.29 / 1.511 ' nrs='0.29 / 1.511 ' sa=0 sb=0 sd=0 mult=1 m=1
Xcibp2 ibp vnc ibpm vss sky130_fd_pr__nfet_g5v0d10v5 L=1 W=1.511 nf=1 ad='int((1 + 1)/2) * 1.511 / 1 * 0.29'
+ as='int((1 + 2)/2) * 1.511 / 1 * 0.29' pd='2*int((1 + 1)/2) * (1.511 / 1 + 0.29)' ps='2*int((1 + 2)/2) * (1.511 / 1 + 0.29)'
+ nrd='0.29 / 1.511 ' nrs='0.29 / 1.511 ' sa=0 sb=0 sd=0 mult=1 m=1
Xmivbl00 ivbl0m vn vss vss sky130_fd_pr__nfet_g5v0d10v5 L=4 W=1.837 nf=1 ad='int((1 + 1)/2) * 1.837 / 1 * 0.29'
+ as='int((1 + 2)/2) * 1.837 / 1 * 0.29' pd='2*int((1 + 1)/2) * (1.837 / 1 + 0.29)' ps='2*int((1 + 2)/2) * (1.837 / 1 + 0.29)'
+ nrd='0.29 / 1.837 ' nrs='0.29 / 1.837 ' sa=0 sb=0 sd=0 mult=1 m=1
Xcivbl00 ivbl0 vnc ivbl0m vss sky130_fd_pr__nfet_g5v0d10v5 L=1 W=1.837 nf=1 ad='int((1 + 1)/2) * 1.837 / 1 * 0.29'
+ as='int((1 + 2)/2) * 1.837 / 1 * 0.29' pd='2*int((1 + 1)/2) * (1.837 / 1 + 0.29)' ps='2*int((1 + 2)/2) * (1.837 / 1 + 0.29)'
+ nrd='0.29 / 1.837 ' nrs='0.29 / 1.837 ' sa=0 sb=0 sd=0 mult=1 m=1
Xmfm vfm vn vss vss sky130_fd_pr__nfet_g5v0d10v5 L=4 W=2 nf=1 ad='int((1 + 1)/2) * 2 / 1 * 0.29' as='int((1 + 2)/2) * 2 / 1 * 0.29'
+ pd='2*int((1 + 1)/2) * (2 / 1 + 0.29)' ps='2*int((1 + 2)/2) * (2 / 1 + 0.29)' nrd='0.29 / 2 ' nrs='0.29 / 2 '
+ sa=0 sb=0 sd=0 mult=1 m=1
Xmfc vp vnc vfm vss sky130_fd_pr__nfet_g5v0d10v5 L=1 W=2 nf=1 ad='int((1 + 1)/2) * 2 / 1 * 0.29' as='int((1 + 2)/2) * 2 / 1 * 0.29'
+ pd='2*int((1 + 1)/2) * (2 / 1 + 0.29)' ps='2*int((1 + 2)/2) * (2 / 1 + 0.29)' nrd='0.29 / 2 ' nrs='0.29 / 2 '
+ sa=0 sb=0 sd=0 mult=1 m=1
Xmvp vp vp vdd vdd sky130_fd_pr__pfet_g5v0d10v5 L=16 W=2 nf=1 ad='int((1 + 1)/2) * 2 / 1 * 0.29' as='int((1 + 2)/2) * 2 / 1 * 0.29'
+ pd='2*int((1 + 1)/2) * (2 / 1 + 0.29)' ps='2*int((1 + 2)/2) * (2 / 1 + 0.29)' nrd='0.29 / 2 ' nrs='0.29 / 2 '
+ sa=0 sb=0 sd=0 mult=2 m=2
Xmibn0 ibn vp vdd vdd sky130_fd_pr__pfet_g5v0d10v5 L=16 W=2 nf=1 ad='int((1 + 1)/2) * 2 / 1 * 0.29' as='int((1 + 2)/2) * 2 / 1 * 0.29'
+ pd='2*int((1 + 1)/2) * (2 / 1 + 0.29)' ps='2*int((1 + 2)/2) * (2 / 1 + 0.29)' nrd='0.29 / 2 ' nrs='0.29 / 2 '
+ sa=0 sb=0 sd=0 mult=1 m=1
Xmibn1 ibn vp vdd vdd sky130_fd_pr__pfet_g5v0d10v5 L=16 W=2 nf=1 ad='int((1 + 1)/2) * 2 / 1 * 0.29' as='int((1 + 2)/2) * 2 / 1 * 0.29'
+ pd='2*int((1 + 1)/2) * (2 / 1 + 0.29)' ps='2*int((1 + 2)/2) * (2 / 1 + 0.29)' nrd='0.29 / 2 ' nrs='0.29 / 2 '
+ sa=0 sb=0 sd=0 mult=1 m=1
Xmibn2 ibn vp vdd vdd sky130_fd_pr__pfet_g5v0d10v5 L=16 W=2 nf=1 ad='int((1 + 1)/2) * 2 / 1 * 0.29' as='int((1 + 2)/2) * 2 / 1 * 0.29'
+ pd='2*int((1 + 1)/2) * (2 / 1 + 0.29)' ps='2*int((1 + 2)/2) * (2 / 1 + 0.29)' nrd='0.29 / 2 ' nrs='0.29 / 2 '
+ sa=0 sb=0 sd=0 mult=1 m=1
Xmibn3 ibn vp vdd vdd sky130_fd_pr__pfet_g5v0d10v5 L=16 W=2 nf=1 ad='int((1 + 1)/2) * 2 / 1 * 0.29' as='int((1 + 2)/2) * 2 / 1 * 0.29'
+ pd='2*int((1 + 1)/2) * (2 / 1 + 0.29)' ps='2*int((1 + 2)/2) * (2 / 1 + 0.29)' nrd='0.29 / 2 ' nrs='0.29 / 2 '
+ sa=0 sb=0 sd=0 mult=1 m=1
Xmibn4 ibn vp vdd vdd sky130_fd_pr__pfet_g5v0d10v5 L=16 W=2 nf=1 ad='int((1 + 1)/2) * 2 / 1 * 0.29' as='int((1 + 2)/2) * 2 / 1 * 0.29'
+ pd='2*int((1 + 1)/2) * (2 / 1 + 0.29)' ps='2*int((1 + 2)/2) * (2 / 1 + 0.29)' nrd='0.29 / 2 ' nrs='0.29 / 2 '
+ sa=0 sb=0 sd=0 mult=1 m=1
Xmibn5 ibn vp vdd vdd sky130_fd_pr__pfet_g5v0d10v5 L=16 W=2 nf=1 ad='int((1 + 1)/2) * 2 / 1 * 0.29' as='int((1 + 2)/2) * 2 / 1 * 0.29'
+ pd='2*int((1 + 1)/2) * (2 / 1 + 0.29)' ps='2*int((1 + 2)/2) * (2 / 1 + 0.29)' nrd='0.29 / 2 ' nrs='0.29 / 2 '
+ sa=0 sb=0 sd=0 mult=1 m=1
Xmibn6 ibn vp vdd vdd sky130_fd_pr__pfet_g5v0d10v5 L=16 W=2 nf=1 ad='int((1 + 1)/2) * 2 / 1 * 0.29' as='int((1 + 2)/2) * 2 / 1 * 0.29'
+ pd='2*int((1 + 1)/2) * (2 / 1 + 0.29)' ps='2*int((1 + 2)/2) * (2 / 1 + 0.29)' nrd='0.29 / 2 ' nrs='0.29 / 2 '
+ sa=0 sb=0 sd=0 mult=1 m=1
Xmibn7 ibn vp vdd vdd sky130_fd_pr__pfet_g5v0d10v5 L=16 W=2 nf=1 ad='int((1 + 1)/2) * 2 / 1 * 0.29' as='int((1 + 2)/2) * 2 / 1 * 0.29'
+ pd='2*int((1 + 1)/2) * (2 / 1 + 0.29)' ps='2*int((1 + 2)/2) * (2 / 1 + 0.29)' nrd='0.29 / 2 ' nrs='0.29 / 2 '
+ sa=0 sb=0 sd=0 mult=1 m=1
Xmibn8 ibn vp vdd vdd sky130_fd_pr__pfet_g5v0d10v5 L=16 W=2 nf=1 ad='int((1 + 1)/2) * 2 / 1 * 0.29' as='int((1 + 2)/2) * 2 / 1 * 0.29'
+ pd='2*int((1 + 1)/2) * (2 / 1 + 0.29)' ps='2*int((1 + 2)/2) * (2 / 1 + 0.29)' nrd='0.29 / 2 ' nrs='0.29 / 2 '
+ sa=0 sb=0 sd=0 mult=1 m=1
Xmibn9 ibn vp vdd vdd sky130_fd_pr__pfet_g5v0d10v5 L=16 W=2 nf=1 ad='int((1 + 1)/2) * 2 / 1 * 0.29' as='int((1 + 2)/2) * 2 / 1 * 0.29'
+ pd='2*int((1 + 1)/2) * (2 / 1 + 0.29)' ps='2*int((1 + 2)/2) * (2 / 1 + 0.29)' nrd='0.29 / 2 ' nrs='0.29 / 2 '
+ sa=0 sb=0 sd=0 mult=1 m=1
Xmibn10 ibn vp vdd vdd sky130_fd_pr__pfet_g5v0d10v5 L=16 W=2 nf=1 ad='int((1 + 1)/2) * 2 / 1 * 0.29'
+ as='int((1 + 2)/2) * 2 / 1 * 0.29' pd='2*int((1 + 1)/2) * (2 / 1 + 0.29)' ps='2*int((1 + 2)/2) * (2 / 1 + 0.29)'
+ nrd='0.29 / 2 ' nrs='0.29 / 2 ' sa=0 sb=0 sd=0 mult=1 m=1
Xmibn11 ibn vp vdd vdd sky130_fd_pr__pfet_g5v0d10v5 L=16 W=1.341 nf=1 ad='int((1 + 1)/2) * 1.341 / 1 * 0.29'
+ as='int((1 + 2)/2) * 1.341 / 1 * 0.29' pd='2*int((1 + 1)/2) * (1.341 / 1 + 0.29)' ps='2*int((1 + 2)/2) * (1.341 / 1 + 0.29)'
+ nrd='0.29 / 1.341 ' nrs='0.29 / 1.341 ' sa=0 sb=0 sd=0 mult=1 m=1
**.ends
.end
